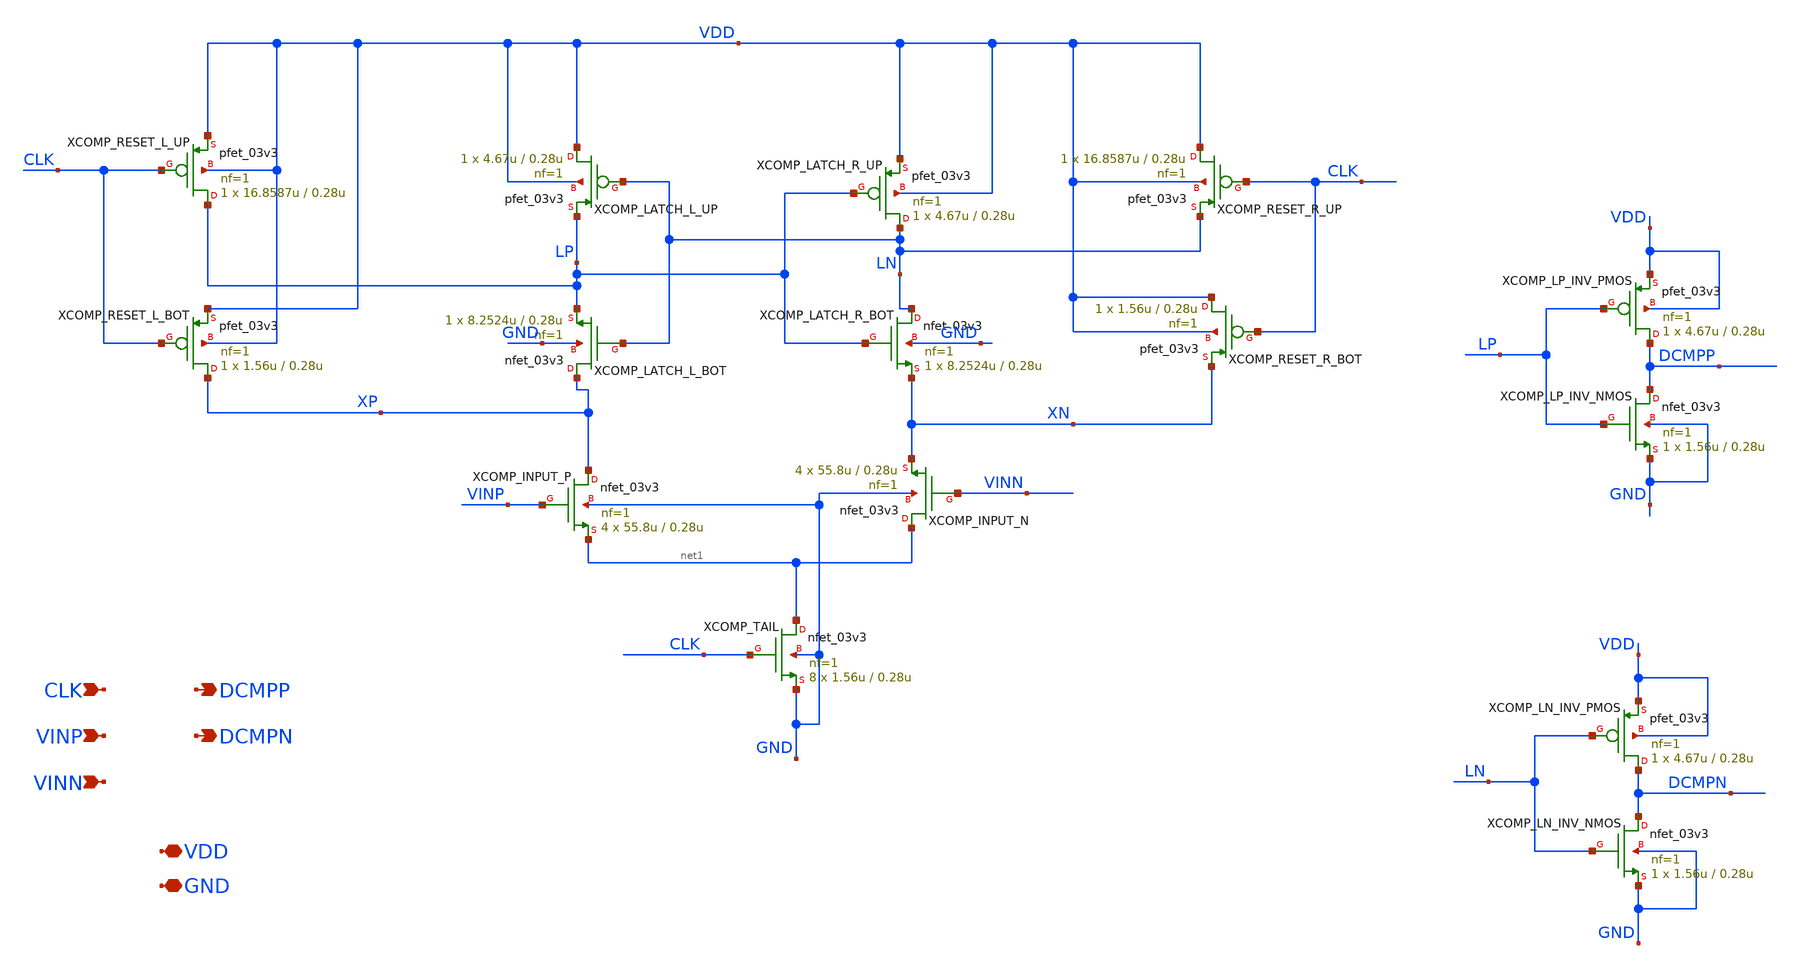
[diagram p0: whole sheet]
** sch_path: verification/a44_w5p29_trans_driver/01_CURRENT_CIRCUIT_FILES/xschem/A44_Comparator_StrongARM.sch
**.subckt A44_Comparator_StrongARM CLK VINP VINN DCMPP DCMPN VDD GND
*.ipin CLK
*.ipin VINP
*.ipin VINN
*.opin DCMPP
*.opin DCMPN
*.iopin VDD
*.iopin GND
XCOMP_TAIL net1 CLK GND GND nfet_03v3 L=0.28u W=1.56u nf=1 ad='int((nf+1)/2) * W/nf * 0.18u' as='int((nf+2)/2) * W/nf * 0.18u'
+ pd='2*int((nf+1)/2) * (W/nf + 0.18u)' ps='2*int((nf+2)/2) * (W/nf + 0.18u)' nrd='0.18u / W' nrs='0.18u / W'
+ sa=0 sb=0 sd=0 m=8
XCOMP_RESET_L_BOT XP CLK VDD VDD pfet_03v3 L=0.28u W=1.56u nf=1 ad='int((nf+1)/2) * W/nf * 0.18u' as='int((nf+2)/2) * W/nf * 0.18u'
+ pd='2*int((nf+1)/2) * (W/nf + 0.18u)' ps='2*int((nf+2)/2) * (W/nf + 0.18u)' nrd='0.18u / W' nrs='0.18u / W'
+ sa=0 sb=0 sd=0 m=1
XCOMP_INPUT_P XP VINP net1 GND nfet_03v3 L=0.28u W=55.8u nf=1 ad='int((nf+1)/2) * W/nf * 0.18u' as='int((nf+2)/2) * W/nf * 0.18u'
+ pd='2*int((nf+1)/2) * (W/nf + 0.18u)' ps='2*int((nf+2)/2) * (W/nf + 0.18u)' nrd='0.18u / W' nrs='0.18u / W'
+ sa=0 sb=0 sd=0 m=4
XCOMP_INPUT_N net1 VINN XN GND nfet_03v3 L=0.28u W=55.8u nf=1 ad='int((nf+1)/2) * W/nf * 0.18u' as='int((nf+2)/2) * W/nf * 0.18u'
+ pd='2*int((nf+1)/2) * (W/nf + 0.18u)' ps='2*int((nf+2)/2) * (W/nf + 0.18u)' nrd='0.18u / W' nrs='0.18u / W'
+ sa=0 sb=0 sd=0 m=4
XCOMP_LATCH_L_BOT XP LN LP GND nfet_03v3 L=0.28u W=8.2524u nf=1 ad='int((nf+1)/2) * W/nf * 0.18u' as='int((nf+2)/2) * W/nf * 0.18u'
+ pd='2*int((nf+1)/2) * (W/nf + 0.18u)' ps='2*int((nf+2)/2) * (W/nf + 0.18u)' nrd='0.18u / W' nrs='0.18u / W'
+ sa=0 sb=0 sd=0 m=1
XCOMP_LATCH_R_BOT LN LP XN GND nfet_03v3 L=0.28u W=8.2524u nf=1 ad='int((nf+1)/2) * W/nf * 0.18u' as='int((nf+2)/2) * W/nf * 0.18u'
+ pd='2*int((nf+1)/2) * (W/nf + 0.18u)' ps='2*int((nf+2)/2) * (W/nf + 0.18u)' nrd='0.18u / W' nrs='0.18u / W'
+ sa=0 sb=0 sd=0 m=1
XCOMP_RESET_L_UP LP CLK VDD VDD pfet_03v3 L=0.28u W=16.8587u nf=1 ad='int((nf+1)/2) * W/nf * 0.18u' as='int((nf+2)/2) * W/nf * 0.18u'
+ pd='2*int((nf+1)/2) * (W/nf + 0.18u)' ps='2*int((nf+2)/2) * (W/nf + 0.18u)' nrd='0.18u / W' nrs='0.18u / W'
+ sa=0 sb=0 sd=0 m=1
XCOMP_LATCH_L_UP VDD LN LP VDD pfet_03v3 L=0.28u W=4.67u nf=1 ad='int((nf+1)/2) * W/nf * 0.18u' as='int((nf+2)/2) * W/nf * 0.18u'
+ pd='2*int((nf+1)/2) * (W/nf + 0.18u)' ps='2*int((nf+2)/2) * (W/nf + 0.18u)' nrd='0.18u / W' nrs='0.18u / W'
+ sa=0 sb=0 sd=0 m=1
XCOMP_LATCH_R_UP LN LP VDD VDD pfet_03v3 L=0.28u W=4.67u nf=1 ad='int((nf+1)/2) * W/nf * 0.18u' as='int((nf+2)/2) * W/nf * 0.18u'
+ pd='2*int((nf+1)/2) * (W/nf + 0.18u)' ps='2*int((nf+2)/2) * (W/nf + 0.18u)' nrd='0.18u / W' nrs='0.18u / W'
+ sa=0 sb=0 sd=0 m=1
XCOMP_RESET_R_BOT VDD CLK XN VDD pfet_03v3 L=0.28u W=1.56u nf=1 ad='int((nf+1)/2) * W/nf * 0.18u' as='int((nf+2)/2) * W/nf * 0.18u'
+ pd='2*int((nf+1)/2) * (W/nf + 0.18u)' ps='2*int((nf+2)/2) * (W/nf + 0.18u)' nrd='0.18u / W' nrs='0.18u / W'
+ sa=0 sb=0 sd=0 m=1
XCOMP_RESET_R_UP VDD CLK LN VDD pfet_03v3 L=0.28u W=16.8587u nf=1 ad='int((nf+1)/2) * W/nf * 0.18u' as='int((nf+2)/2) * W/nf * 0.18u'
+ pd='2*int((nf+1)/2) * (W/nf + 0.18u)' ps='2*int((nf+2)/2) * (W/nf + 0.18u)' nrd='0.18u / W' nrs='0.18u / W'
+ sa=0 sb=0 sd=0 m=1
XCOMP_LN_INV_PMOS DCMPN LN VDD VDD pfet_03v3 L=0.28u W=4.67u nf=1 ad='int((nf+1)/2) * W/nf * 0.18u' as='int((nf+2)/2) * W/nf * 0.18u'
+ pd='2*int((nf+1)/2) * (W/nf + 0.18u)' ps='2*int((nf+2)/2) * (W/nf + 0.18u)' nrd='0.18u / W' nrs='0.18u / W'
+ sa=0 sb=0 sd=0 m=1
XCOMP_LN_INV_NMOS DCMPN LN GND GND nfet_03v3 L=0.28u W=1.56u nf=1 ad='int((nf+1)/2) * W/nf * 0.18u' as='int((nf+2)/2) * W/nf * 0.18u'
+ pd='2*int((nf+1)/2) * (W/nf + 0.18u)' ps='2*int((nf+2)/2) * (W/nf + 0.18u)' nrd='0.18u / W' nrs='0.18u / W'
+ sa=0 sb=0 sd=0 m=1
XCOMP_LP_INV_PMOS DCMPP LP VDD VDD pfet_03v3 L=0.28u W=4.67u nf=1 ad='int((nf+1)/2) * W/nf * 0.18u' as='int((nf+2)/2) * W/nf * 0.18u'
+ pd='2*int((nf+1)/2) * (W/nf + 0.18u)' ps='2*int((nf+2)/2) * (W/nf + 0.18u)' nrd='0.18u / W' nrs='0.18u / W'
+ sa=0 sb=0 sd=0 m=1
XCOMP_LP_INV_NMOS DCMPP LP GND GND nfet_03v3 L=0.28u W=1.56u nf=1 ad='int((nf+1)/2) * W/nf * 0.18u' as='int((nf+2)/2) * W/nf * 0.18u'
+ pd='2*int((nf+1)/2) * (W/nf + 0.18u)' ps='2*int((nf+2)/2) * (W/nf + 0.18u)' nrd='0.18u / W' nrs='0.18u / W'
+ sa=0 sb=0 sd=0 m=1
**.ends
.end
